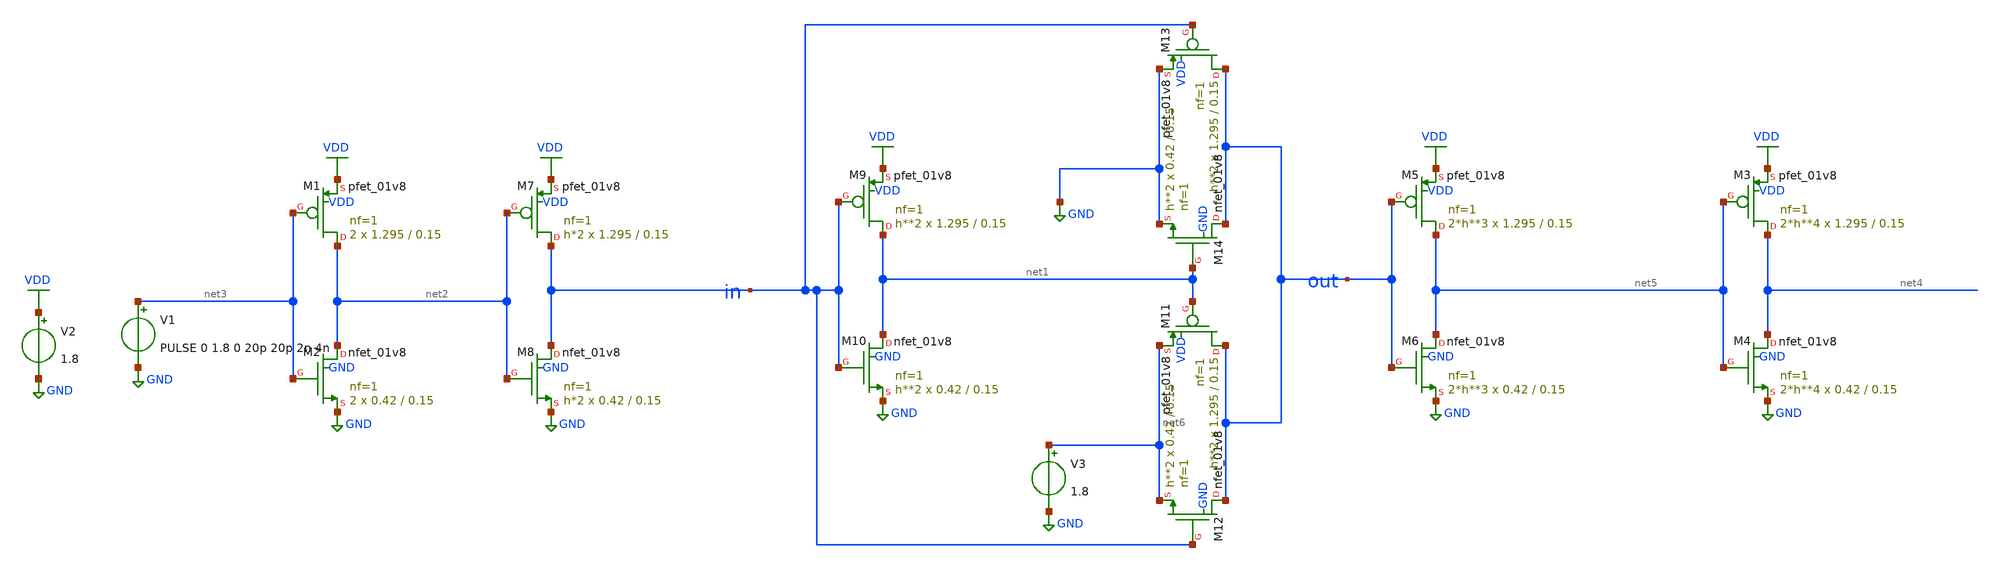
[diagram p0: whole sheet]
** sch_path: transmission_gate/logicaleffort/tg_2.sch
**.subckt tg_2
XM13 out in GND VDD sky130_fd_pr__pfet_01v8 L=0.15 W=1.295 nf=1 ad='int((1 + 1)/2) * 1.295 / 1 * 0.29'
+ as='int((1 + 2)/2) * 1.295 / 1 * 0.29' pd='2*int((1 + 1)/2) * (1.295 / 1 + 0.29)' ps='2*int((1 + 2)/2) * (1.295 / 1 + 0.29)'
+ nrd='0.29 / 1.295 ' nrs='0.29 / 1.295 ' sa=0 sb=0 sd=0 mult=h**2 m=h**2
XM14 out net1 GND GND sky130_fd_pr__nfet_01v8 L=0.15 W=0.42 nf=1 ad='int((1 + 1)/2) * 0.42 / 1 * 0.29'
+ as='int((1 + 2)/2) * 0.42 / 1 * 0.29' pd='2*int((1 + 1)/2) * (0.42 / 1 + 0.29)' ps='2*int((1 + 2)/2) * (0.42 / 1 + 0.29)'
+ nrd='0.29 / 0.42 ' nrs='0.29 / 0.42 ' sa=0 sb=0 sd=0 mult=h**2 m=h**2
XM9 net1 in VDD VDD sky130_fd_pr__pfet_01v8 L=0.15 W=1.295 nf=1 ad='int((1 + 1)/2) * 1.295 / 1 * 0.29'
+ as='int((1 + 2)/2) * 1.295 / 1 * 0.29' pd='2*int((1 + 1)/2) * (1.295 / 1 + 0.29)' ps='2*int((1 + 2)/2) * (1.295 / 1 + 0.29)'
+ nrd='0.29 / 1.295 ' nrs='0.29 / 1.295 ' sa=0 sb=0 sd=0 mult=h**2 m=h**2
XM10 net1 in GND GND sky130_fd_pr__nfet_01v8 L=0.15 W=0.42 nf=1 ad='int((1 + 1)/2) * 0.42 / 1 * 0.29'
+ as='int((1 + 2)/2) * 0.42 / 1 * 0.29' pd='2*int((1 + 1)/2) * (0.42 / 1 + 0.29)' ps='2*int((1 + 2)/2) * (0.42 / 1 + 0.29)'
+ nrd='0.29 / 0.42 ' nrs='0.29 / 0.42 ' sa=0 sb=0 sd=0 mult=h**2 m=h**2
XM1 net2 net3 VDD VDD sky130_fd_pr__pfet_01v8 L=0.15 W=1.295 nf=1 ad='int((1 + 1)/2) * 1.295 / 1 * 0.29'
+ as='int((1 + 2)/2) * 1.295 / 1 * 0.29' pd='2*int((1 + 1)/2) * (1.295 / 1 + 0.29)' ps='2*int((1 + 2)/2) * (1.295 / 1 + 0.29)'
+ nrd='0.29 / 1.295 ' nrs='0.29 / 1.295 ' sa=0 sb=0 sd=0 mult=2 m=2
XM2 net2 net3 GND GND sky130_fd_pr__nfet_01v8 L=0.15 W=0.42 nf=1 ad='int((1 + 1)/2) * 0.42 / 1 * 0.29'
+ as='int((1 + 2)/2) * 0.42 / 1 * 0.29' pd='2*int((1 + 1)/2) * (0.42 / 1 + 0.29)' ps='2*int((1 + 2)/2) * (0.42 / 1 + 0.29)'
+ nrd='0.29 / 0.42 ' nrs='0.29 / 0.42 ' sa=0 sb=0 sd=0 mult=2 m=2
XM3 net4 net5 VDD VDD sky130_fd_pr__pfet_01v8 L=0.15 W=1.295 nf=1 ad='int((1 + 1)/2) * 1.295 / 1 * 0.29'
+ as='int((1 + 2)/2) * 1.295 / 1 * 0.29' pd='2*int((1 + 1)/2) * (1.295 / 1 + 0.29)' ps='2*int((1 + 2)/2) * (1.295 / 1 + 0.29)'
+ nrd='0.29 / 1.295 ' nrs='0.29 / 1.295 ' sa=0 sb=0 sd=0 mult=2*h**4 m=2*h**4
XM4 net4 net5 GND GND sky130_fd_pr__nfet_01v8 L=0.15 W=0.42 nf=1 ad='int((1 + 1)/2) * 0.42 / 1 * 0.29'
+ as='int((1 + 2)/2) * 0.42 / 1 * 0.29' pd='2*int((1 + 1)/2) * (0.42 / 1 + 0.29)' ps='2*int((1 + 2)/2) * (0.42 / 1 + 0.29)'
+ nrd='0.29 / 0.42 ' nrs='0.29 / 0.42 ' sa=0 sb=0 sd=0 mult=2*h**4 m=2*h**4
XM5 net5 out VDD VDD sky130_fd_pr__pfet_01v8 L=0.15 W=1.295 nf=1 ad='int((1 + 1)/2) * 1.295 / 1 * 0.29'
+ as='int((1 + 2)/2) * 1.295 / 1 * 0.29' pd='2*int((1 + 1)/2) * (1.295 / 1 + 0.29)' ps='2*int((1 + 2)/2) * (1.295 / 1 + 0.29)'
+ nrd='0.29 / 1.295 ' nrs='0.29 / 1.295 ' sa=0 sb=0 sd=0 mult=2*h**3 m=2*h**3
XM6 net5 out GND GND sky130_fd_pr__nfet_01v8 L=0.15 W=0.42 nf=1 ad='int((1 + 1)/2) * 0.42 / 1 * 0.29'
+ as='int((1 + 2)/2) * 0.42 / 1 * 0.29' pd='2*int((1 + 1)/2) * (0.42 / 1 + 0.29)' ps='2*int((1 + 2)/2) * (0.42 / 1 + 0.29)'
+ nrd='0.29 / 0.42 ' nrs='0.29 / 0.42 ' sa=0 sb=0 sd=0 mult=2*h**3 m=2*h**3
V1 net3 GND PULSE 0 1.8 0 20p 20p 2n 4n
V2 VDD GND 1.8
XM7 in net2 VDD VDD sky130_fd_pr__pfet_01v8 L=0.15 W=1.295 nf=1 ad='int((1 + 1)/2) * 1.295 / 1 * 0.29'
+ as='int((1 + 2)/2) * 1.295 / 1 * 0.29' pd='2*int((1 + 1)/2) * (1.295 / 1 + 0.29)' ps='2*int((1 + 2)/2) * (1.295 / 1 + 0.29)'
+ nrd='0.29 / 1.295 ' nrs='0.29 / 1.295 ' sa=0 sb=0 sd=0 mult=h*2 m=h*2
XM8 in net2 GND GND sky130_fd_pr__nfet_01v8 L=0.15 W=0.42 nf=1 ad='int((1 + 1)/2) * 0.42 / 1 * 0.29'
+ as='int((1 + 2)/2) * 0.42 / 1 * 0.29' pd='2*int((1 + 1)/2) * (0.42 / 1 + 0.29)' ps='2*int((1 + 2)/2) * (0.42 / 1 + 0.29)'
+ nrd='0.29 / 0.42 ' nrs='0.29 / 0.42 ' sa=0 sb=0 sd=0 mult=h*2 m=h*2
XM11 out net1 net6 VDD sky130_fd_pr__pfet_01v8 L=0.15 W=1.295 nf=1 ad='int((1 + 1)/2) * 1.295 / 1 * 0.29'
+ as='int((1 + 2)/2) * 1.295 / 1 * 0.29' pd='2*int((1 + 1)/2) * (1.295 / 1 + 0.29)' ps='2*int((1 + 2)/2) * (1.295 / 1 + 0.29)'
+ nrd='0.29 / 1.295 ' nrs='0.29 / 1.295 ' sa=0 sb=0 sd=0 mult=h**2 m=h**2
XM12 out in net6 GND sky130_fd_pr__nfet_01v8 L=0.15 W=0.42 nf=1 ad='int((1 + 1)/2) * 0.42 / 1 * 0.29'
+ as='int((1 + 2)/2) * 0.42 / 1 * 0.29' pd='2*int((1 + 1)/2) * (0.42 / 1 + 0.29)' ps='2*int((1 + 2)/2) * (0.42 / 1 + 0.29)'
+ nrd='0.29 / 0.42 ' nrs='0.29 / 0.42 ' sa=0 sb=0 sd=0 mult=h**2 m=h**2
V3 net6 GND 1.8
**** begin user architecture code


.lib /usr/local/share/pdk/sky130A/libs.tech/ngspice/sky130.lib.spice tt
.param h = 0
.control
save in out
  let start = 1
  let stop = 8
  let step = 1
  let cur = start
  let n = ((stop - start) / step) + 1
  let hall = unitvec(n)
  let tpdrall = unitvec(n)
  let tpdfall = unitvec(n)
  let tpdall = unitvec(n)
  let diffall = unitvec(n)
  let m = 0
  while m < n
    let hv = cur
    alterparam h = $&hv
    reset
    tran 0.1p 20n
    meas tran tpdr trig v(in) val=0.9 rise=1 targ v(out) val=0.9 rise=1
    meas tran tpdf trig v(in) val=0.9 fall=1 targ v(out) val=0.9 fall=1
    let hall[m] = hv
    let tpdrall[m] = tpdr
    let tpdfall[m] = tpdf
    let tpdall[m] = (tpdr + tpdf) / 2
    let diffall[m] = abs(tpdr - tpdf)
    let cur = cur + step
    let m = m + 1
  end
  meas tran tr trig v(in) val = 0.18 rise=1 targ v(in) val=1.62 rise=1
  meas tran tf trig v(in) val = 1.62 fall=1 targ v(in) val=0.18 fall=1
  print hall tpdrall tpdfall tpdall diffall
.endc


**** end user architecture code
**.ends
.GLOBAL GND
.GLOBAL VDD
.end
